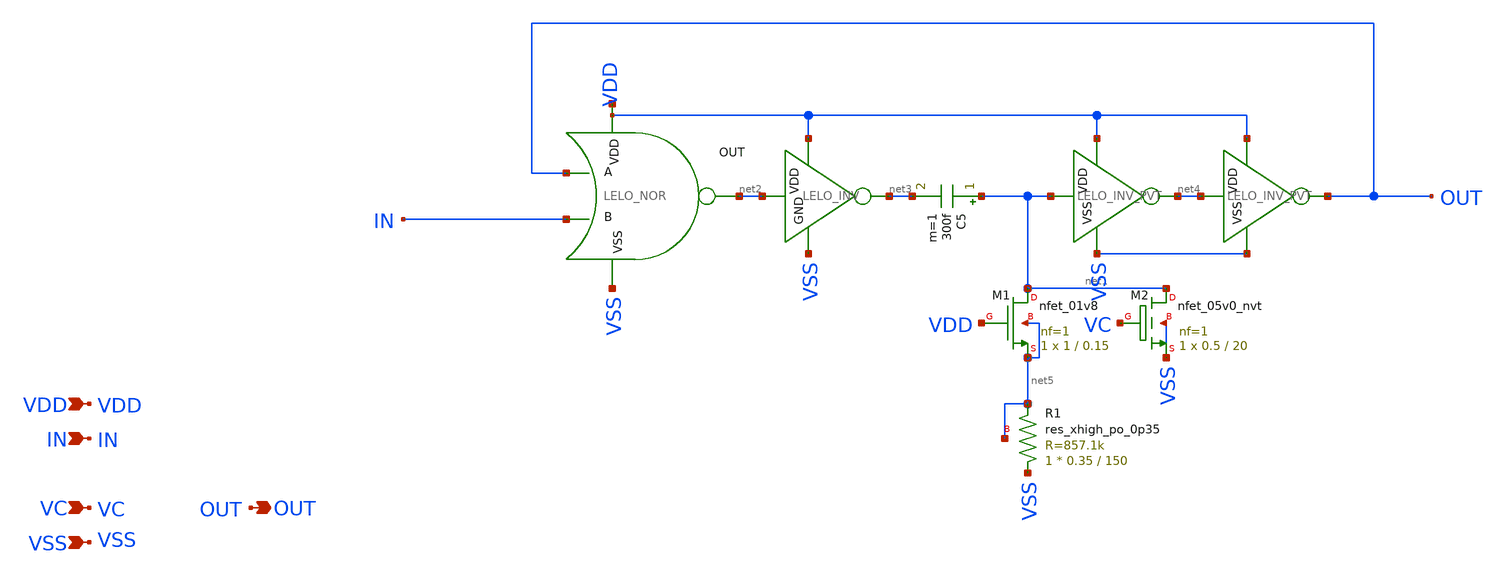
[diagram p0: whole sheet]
** sch_path: design/LELO_SVOD_SKY130A/LELO_ONESHOT_VC.sch
**.subckt LELO_ONESHOT_VC VDD IN VC VSS OUT
*.ipin VDD
*.ipin IN
*.ipin VC
*.ipin VSS
*.opin OUT
x2 net6 net2 OUT IN VSS LELO_NOR
C5 net1 net3 300f m=1
XM1 net1 VDD net5 net5 sky130_fd_pr__nfet_01v8 L=0.15 W=1 nf=1 ad='int((1 + 1)/2) * 1 / 1 * 0.29' as='int((1 + 2)/2) * 1 / 1 * 0.29'
+ pd='2*int((1 + 1)/2) * (1 / 1 + 0.29)' ps='2*int((1 + 2)/2) * (1 / 1 + 0.29)' nrd='0.29 / 1 ' nrs='0.29 / 1 '
+ sa=0 sb=0 sd=0 mult=1 m=1
XM2 net1 VC VSS VSS sky130_fd_pr__nfet_05v0_nvt L=20 W=0.5 nf=1 ad='int((1 + 1)/2) * 0.5 / 1 * 0.29'
+ as='int((1 + 2)/2) * 0.5 / 1 * 0.29' pd='2*int((1 + 1)/2) * (0.5 / 1 + 0.29)' ps='2*int((1 + 2)/2) * (0.5 / 1 + 0.29)'
+ nrd='0.29 / 0.5 ' nrs='0.29 / 0.5 ' sa=0 sb=0 sd=0 mult=1 m=1
XR1 VSS net5 net5 sky130_fd_pr__res_xhigh_po_0p35 L=150 mult=1 m=1
x1 VDD net1 net4 VSS LELO_INV_PVT
x3 VDD net4 OUT VSS LELO_INV_PVT
x4 VDD net2 net3 VSS LELO_INV
**.ends

* expanding   symbol:  LELO_SVOD_SKY130A/LELO_NOR.sym # of pins=5
** sym_path: design/LELO_SVOD_SKY130A/LELO_NOR.sym
** sch_path: design/LELO_SVOD_SKY130A/LELO_NOR.sch
.subckt LELO_NOR VDD OUT A B VSS
*.ipin VDD
*.ipin VSS
*.opin OUT
*.ipin A
*.ipin B
XM2 OUT B VSS VSS sky130_fd_pr__nfet_01v8 L=0.15 W=2 nf=1 ad='int((1 + 1)/2) * 2 / 1 * 0.29' as='int((1 + 2)/2) * 2 / 1 * 0.29'
+ pd='2*int((1 + 1)/2) * (2 / 1 + 0.29)' ps='2*int((1 + 2)/2) * (2 / 1 + 0.29)' nrd='0.29 / 2 ' nrs='0.29 / 2 '
+ sa=0 sb=0 sd=0 mult=1 m=1
XM1 OUT A VSS VSS sky130_fd_pr__nfet_01v8 L=0.15 W=2 nf=1 ad='int((1 + 1)/2) * 2 / 1 * 0.29' as='int((1 + 2)/2) * 2 / 1 * 0.29'
+ pd='2*int((1 + 1)/2) * (2 / 1 + 0.29)' ps='2*int((1 + 2)/2) * (2 / 1 + 0.29)' nrd='0.29 / 2 ' nrs='0.29 / 2 '
+ sa=0 sb=0 sd=0 mult=1 m=1
XM3 OUT B net1 VDD sky130_fd_pr__pfet_01v8 L=0.15 W=4 nf=1 ad='int((1 + 1)/2) * 4 / 1 * 0.29' as='int((1 + 2)/2) * 4 / 1 * 0.29'
+ pd='2*int((1 + 1)/2) * (4 / 1 + 0.29)' ps='2*int((1 + 2)/2) * (4 / 1 + 0.29)' nrd='0.29 / 4 ' nrs='0.29 / 4 '
+ sa=0 sb=0 sd=0 mult=1 m=1
XM4 net1 A VDD VDD sky130_fd_pr__pfet_01v8 L=0.15 W=4 nf=1 ad='int((1 + 1)/2) * 4 / 1 * 0.29' as='int((1 + 2)/2) * 4 / 1 * 0.29'
+ pd='2*int((1 + 1)/2) * (4 / 1 + 0.29)' ps='2*int((1 + 2)/2) * (4 / 1 + 0.29)' nrd='0.29 / 4 ' nrs='0.29 / 4 '
+ sa=0 sb=0 sd=0 mult=1 m=1
.ends


* expanding   symbol:  LELO_SVOD_SKY130A/LELO_INV_PVT.sym # of pins=4
** sym_path: design/LELO_SVOD_SKY130A/LELO_INV_PVT.sym
** sch_path: design/LELO_SVOD_SKY130A/LELO_INV_PVT.sch
.subckt LELO_INV_PVT VDD VIN VOUT VSS
*.ipin VIN
*.ipin VDD
*.ipin VSS
*.opin VOUT
XM1 VOUT VIN VSS VSS sky130_fd_pr__nfet_01v8 L=0.5 W=4 nf=1 ad='int((1 + 1)/2) * 4 / 1 * 0.29' as='int((1 + 2)/2) * 4 / 1 * 0.29'
+ pd='2*int((1 + 1)/2) * (4 / 1 + 0.29)' ps='2*int((1 + 2)/2) * (4 / 1 + 0.29)' nrd='0.29 / 4 ' nrs='0.29 / 4 '
+ sa=0 sb=0 sd=0 mult=1 m=1
XM2 VOUT VIN VDD VDD sky130_fd_pr__pfet_01v8_lvt L=1 W=4 nf=1 ad='int((1 + 1)/2) * 4 / 1 * 0.29' as='int((1 + 2)/2) * 4 / 1 * 0.29'
+ pd='2*int((1 + 1)/2) * (4 / 1 + 0.29)' ps='2*int((1 + 2)/2) * (4 / 1 + 0.29)' nrd='0.29 / 4 ' nrs='0.29 / 4 '
+ sa=0 sb=0 sd=0 mult=1 m=1
.ends


* expanding   symbol:  LELO_SVOD_SKY130A/LELO_INV.sym # of pins=4
** sym_path: design/LELO_SVOD_SKY130A/LELO_INV.sym
** sch_path: design/LELO_SVOD_SKY130A/LELO_INV.sch
.subckt LELO_INV VDD VIN VOUT GND
*.ipin VIN
*.ipin VDD
*.ipin GND
*.opin VOUT
XM1 VOUT VIN GND GND sky130_fd_pr__nfet_01v8_lvt L=0.15 W=1 nf=1 ad='int((1 + 1)/2) * 1 / 1 * 0.29' as='int((1 + 2)/2) * 1 / 1 * 0.29'
+ pd='2*int((1 + 1)/2) * (1 / 1 + 0.29)' ps='2*int((1 + 2)/2) * (1 / 1 + 0.29)' nrd='0.29 / 1 ' nrs='0.29 / 1 '
+ sa=0 sb=0 sd=0 mult=1 m=1
XM2 VOUT VIN VDD VDD sky130_fd_pr__pfet_01v8_lvt L=0.35 W=1 nf=1 ad='int((1 + 1)/2) * 1 / 1 * 0.29' as='int((1 + 2)/2) * 1 / 1 * 0.29'
+ pd='2*int((1 + 1)/2) * (1 / 1 + 0.29)' ps='2*int((1 + 2)/2) * (1 / 1 + 0.29)' nrd='0.29 / 1 ' nrs='0.29 / 1 '
+ sa=0 sb=0 sd=0 mult=2 m=2
.ends

.end
